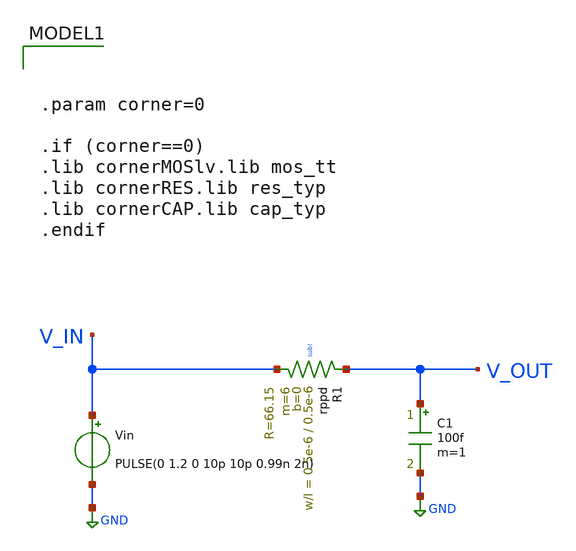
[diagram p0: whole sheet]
** sch_path: others/phase_measurement.sch
**.subckt phase_measurement
C1 V_OUT GND 100f m=1
XR1 V_OUT V_IN sub! rppd w=0.5e-6 l=0.5e-6 m=6 b=0 mm_ok=1
Vin V_IN GND PULSE(0 1.2 0 10p 10p 0.99n 2n)
**** begin user architecture code


.param corner=0

.if (corner==0)
.lib cornerMOSlv.lib mos_tt
.lib cornerRES.lib res_typ
.lib cornerCAP.lib cap_typ
.endif



.control
* ---- settings you tweak ----
   * ---- user settings ----
  let vlow  = 0
  let vhigh = 1.2
  let v50   = vlow + 0.5*(vhigh - vlow)

  let start_edge = 5     ; skip early edges (settling)
  let N = 50             ; number of phase samples

  tran 1p 200n

  * ---- allocate vectors ----
  let tvec   = vector(N)
  let phivec = vector(N)

  let k = 0
  let i = start_edge

  while k < N
    * crossing times
    meas tran tin      WHEN v(v_in)=v50  RISE=i
    meas tran tout     WHEN v(v_out)=v50 RISE=i
    meas tran tin_next WHEN v(v_in)=v50  RISE=(i+1)

    * delay + period
    let dt = tout - tin
    let T  = tin_next - tin

    * phase in degrees (per-cycle)
    let phi = 360*dt/T

    * store sample at time = tin
    let tvec[k]   = tin
    let phivec[k] = phi

    let k = k + 1
    let i = i + 1
  end

  * plot phase vs time (one point per cycle)
  plot phivec vs tvec
.endc


**** end user architecture code
**.ends
.GLOBAL GND
.end
